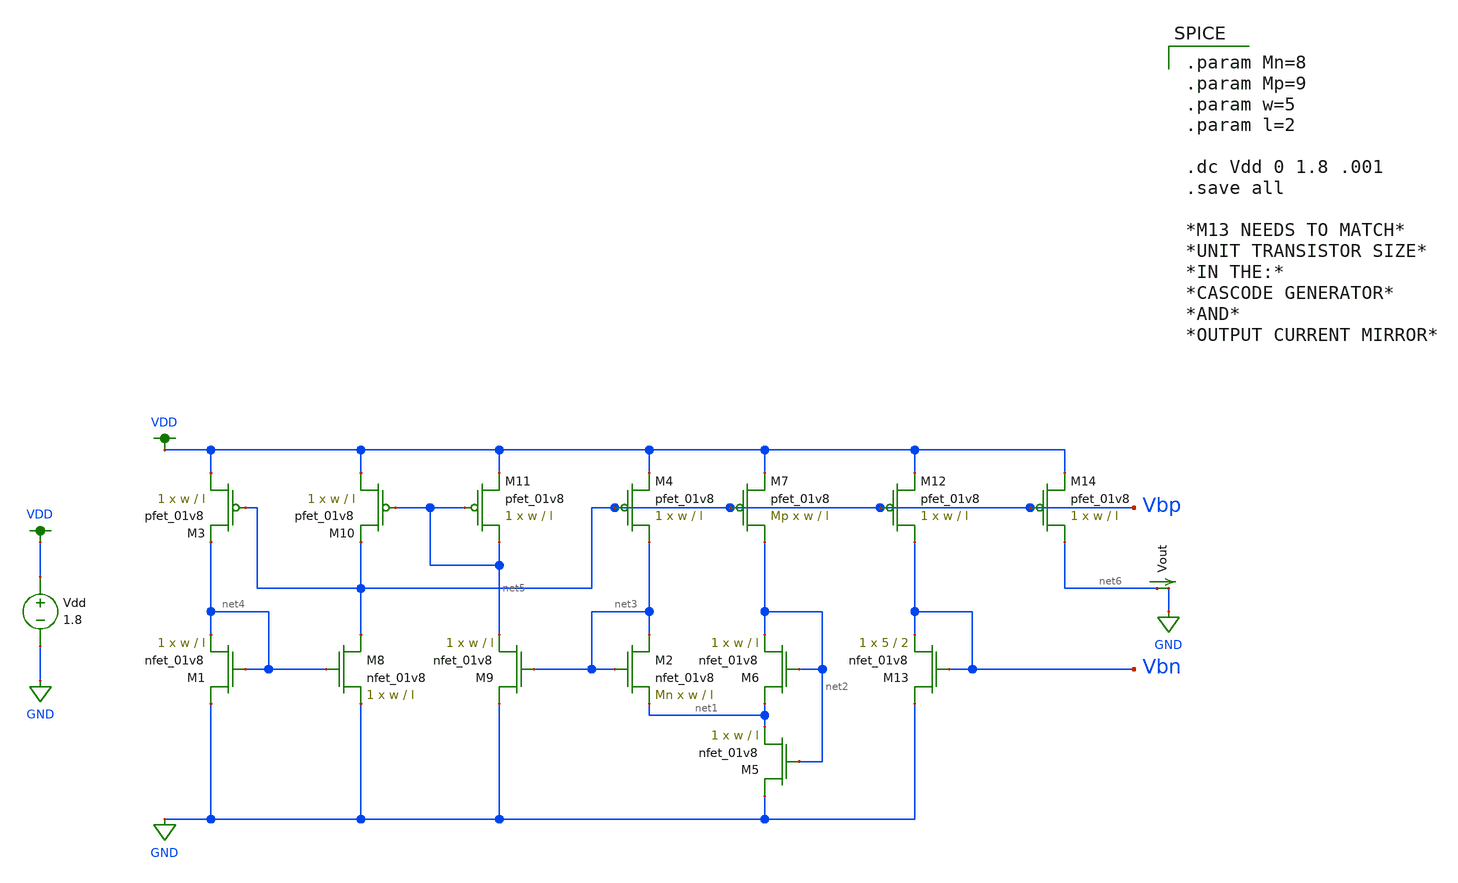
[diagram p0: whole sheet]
** sch_path: schematic/test/bias_current.sch
**.subckt bias_current
XM1 GND net4 net4 GND sky130_fd_pr__nfet_01v8 L=l W=w nf=1 ad='int((nf+1)/2) * W/nf * 0.29' as='int((nf+2)/2) * W/nf * 0.29'
+ pd='2*int((nf+1)/2) * (W/nf + 0.29)' ps='2*int((nf+2)/2) * (W/nf + 0.29)' nrd='0.29 / W' nrs='0.29 / W'
+ sa=0 sb=0 sd=0 mult=1 m=1
XM2 net3 net3 net1 GND sky130_fd_pr__nfet_01v8 L=l W=w nf=1 ad='int((nf+1)/2) * W/nf * 0.29' as='int((nf+2)/2) * W/nf * 0.29'
+ pd='2*int((nf+1)/2) * (W/nf + 0.29)' ps='2*int((nf+2)/2) * (W/nf + 0.29)' nrd='0.29 / W' nrs='0.29 / W'
+ sa=0 sb=0 sd=0 mult=Mn m=Mn
XM3 VDD Vbp net4 VDD sky130_fd_pr__pfet_01v8 L=l W=w nf=1 ad='int((nf+1)/2) * W/nf * 0.29' as='int((nf+2)/2) * W/nf * 0.29'
+ pd='2*int((nf+1)/2) * (W/nf + 0.29)' ps='2*int((nf+2)/2) * (W/nf + 0.29)' nrd='0.29 / W' nrs='0.29 / W'
+ sa=0 sb=0 sd=0 mult=1 m=1
XM4 net3 Vbp VDD VDD sky130_fd_pr__pfet_01v8 L=l W=w nf=1 ad='int((nf+1)/2) * W/nf * 0.29' as='int((nf+2)/2) * W/nf * 0.29'
+ pd='2*int((nf+1)/2) * (W/nf + 0.29)' ps='2*int((nf+2)/2) * (W/nf + 0.29)' nrd='0.29 / W' nrs='0.29 / W'
+ sa=0 sb=0 sd=0 mult=1 m=1
XM5 GND net2 net1 GND sky130_fd_pr__nfet_01v8 L=l W=w nf=1 ad='int((nf+1)/2) * W/nf * 0.29' as='int((nf+2)/2) * W/nf * 0.29'
+ pd='2*int((nf+1)/2) * (W/nf + 0.29)' ps='2*int((nf+2)/2) * (W/nf + 0.29)' nrd='0.29 / W' nrs='0.29 / W'
+ sa=0 sb=0 sd=0 mult=1 m=1
XM6 net1 net2 net2 GND sky130_fd_pr__nfet_01v8 L=l W=w nf=1 ad='int((nf+1)/2) * W/nf * 0.29' as='int((nf+2)/2) * W/nf * 0.29'
+ pd='2*int((nf+1)/2) * (W/nf + 0.29)' ps='2*int((nf+2)/2) * (W/nf + 0.29)' nrd='0.29 / W' nrs='0.29 / W'
+ sa=0 sb=0 sd=0 mult=1 m=1
XM7 net2 Vbp VDD VDD sky130_fd_pr__pfet_01v8 L=l W=w nf=1 ad='int((nf+1)/2) * W/nf * 0.29' as='int((nf+2)/2) * W/nf * 0.29'
+ pd='2*int((nf+1)/2) * (W/nf + 0.29)' ps='2*int((nf+2)/2) * (W/nf + 0.29)' nrd='0.29 / W' nrs='0.29 / W'
+ sa=0 sb=0 sd=0 mult=Mp m=Mp
XM8 Vbp net4 GND GND sky130_fd_pr__nfet_01v8 L=l W=w nf=1 ad='int((nf+1)/2) * W/nf * 0.29' as='int((nf+2)/2) * W/nf * 0.29'
+ pd='2*int((nf+1)/2) * (W/nf + 0.29)' ps='2*int((nf+2)/2) * (W/nf + 0.29)' nrd='0.29 / W' nrs='0.29 / W'
+ sa=0 sb=0 sd=0 mult=1 m=1
XM9 GND net3 net5 GND sky130_fd_pr__nfet_01v8 L=l W=w nf=1 ad='int((nf+1)/2) * W/nf * 0.29' as='int((nf+2)/2) * W/nf * 0.29'
+ pd='2*int((nf+1)/2) * (W/nf + 0.29)' ps='2*int((nf+2)/2) * (W/nf + 0.29)' nrd='0.29 / W' nrs='0.29 / W'
+ sa=0 sb=0 sd=0 mult=1 m=1
XM10 VDD net5 Vbp VDD sky130_fd_pr__pfet_01v8 L=l W=w nf=1 ad='int((nf+1)/2) * W/nf * 0.29' as='int((nf+2)/2) * W/nf * 0.29'
+ pd='2*int((nf+1)/2) * (W/nf + 0.29)' ps='2*int((nf+2)/2) * (W/nf + 0.29)' nrd='0.29 / W' nrs='0.29 / W'
+ sa=0 sb=0 sd=0 mult=1 m=1
XM11 net5 net5 VDD VDD sky130_fd_pr__pfet_01v8 L=l W=w nf=1 ad='int((nf+1)/2) * W/nf * 0.29' as='int((nf+2)/2) * W/nf * 0.29'
+ pd='2*int((nf+1)/2) * (W/nf + 0.29)' ps='2*int((nf+2)/2) * (W/nf + 0.29)' nrd='0.29 / W' nrs='0.29 / W'
+ sa=0 sb=0 sd=0 mult=1 m=1
XM12 Vbn Vbp VDD VDD sky130_fd_pr__pfet_01v8 L=l W=w nf=1 ad='int((nf+1)/2) * W/nf * 0.29' as='int((nf+2)/2) * W/nf * 0.29'
+ pd='2*int((nf+1)/2) * (W/nf + 0.29)' ps='2*int((nf+2)/2) * (W/nf + 0.29)' nrd='0.29 / W' nrs='0.29 / W'
+ sa=0 sb=0 sd=0 mult=1 m=1
XM13 GND Vbn Vbn GND sky130_fd_pr__nfet_01v8 L=2 W=5 nf=1 ad='int((nf+1)/2) * W/nf * 0.29' as='int((nf+2)/2) * W/nf * 0.29'
+ pd='2*int((nf+1)/2) * (W/nf + 0.29)' ps='2*int((nf+2)/2) * (W/nf + 0.29)' nrd='0.29 / W' nrs='0.29 / W'
+ sa=0 sb=0 sd=0 mult=1 m=1
XM14 net6 Vbp VDD VDD sky130_fd_pr__pfet_01v8 L=l W=w nf=1 ad='int((nf+1)/2) * W/nf * 0.29' as='int((nf+2)/2) * W/nf * 0.29'
+ pd='2*int((nf+1)/2) * (W/nf + 0.29)' ps='2*int((nf+2)/2) * (W/nf + 0.29)' nrd='0.29 / W' nrs='0.29 / W'
+ sa=0 sb=0 sd=0 mult=1 m=1
Vout net6 GND 0
.save i(vout)
Vdd VDD GND 1.8
**** begin user architecture code

.param Mn=8
.param Mp=9
.param w=5
.param l=2

.dc Vdd 0 1.8 .001
.save all

*M13 NEEDS TO MATCH*
*UNIT TRANSISTOR SIZE*
*IN THE:*
*CASCODE GENERATOR*
*AND*
*OUTPUT CURRENT MIRROR*


.option wnflag=1
.param MC_SWITCH=0.0
.lib ~/skywater/skywater-pdk/libraries/sky130_fd_pr_ngspice/latest/models/sky130.lib.spice tt

**** end user architecture code
**.ends
.GLOBAL GND
.GLOBAL VDD
.end
